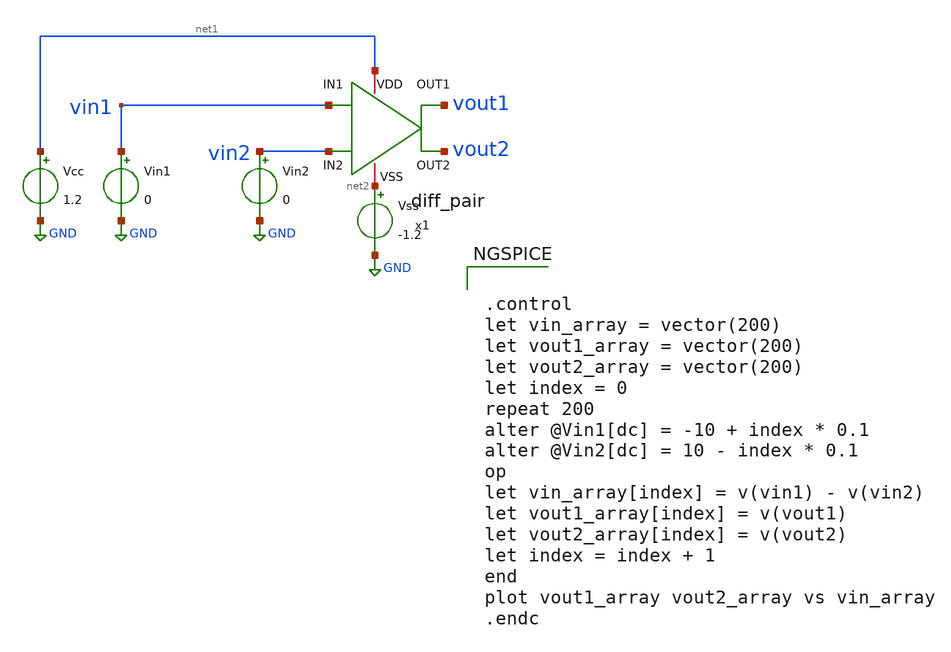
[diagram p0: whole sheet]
** sch_path: xschem/diff_pair_tb.sch
**.subckt diff_pair_tb
Vin2 vin2 GND 0
Vin1 vin1 GND 0
Vcc net1 GND 1.2
x1 net1 vout2 vout1 vin1 vin2 net2 diff_pair
Vss net2 GND -1.2
**** begin user architecture code


.control
let vin_array = vector(200)
let vout1_array = vector(200)
let vout2_array = vector(200)
let index = 0
repeat 200
alter @Vin1[dc] = -10 + index * 0.1
alter @Vin2[dc] = 10 - index * 0.1
op
let vin_array[index] = v(vin1) - v(vin2)
let vout1_array[index] = v(vout1)
let vout2_array[index] = v(vout2)
let index = index + 1
end
plot vout1_array vout2_array vs vin_array
.endc


**** end user architecture code
**.ends

* expanding   symbol:  diff_pair.sym # of pins=6
** sym_path: xschem/diff_pair.sym
** sch_path: xschem/diff_pair.sch
.subckt diff_pair VDD OUT2 OUT1 IN1 IN2 VSS
*.iopin VDD
*.iopin VSS
*.ipin IN1
*.ipin IN2
*.opin OUT2
*.opin OUT1
XM1 OUT1 IN1 net1 net1 sg13_lv_nmos w=1u l=0.13u ng=1 m=1 mm_ok=1
XM2 OUT2 IN2 net1 net1 sg13_lv_nmos w=1u l=0.13u ng=1 m=1 mm_ok=1
I0 net1 VSS 1m
R1 VDD OUT1 1k m=1
R2 VDD OUT2 1k m=1
**** begin user architecture code


.lib cornerMOSlv.lib mos_tt
.lib cornerRES.lib res_typ


**** end user architecture code
.ends

.GLOBAL GND
.end
